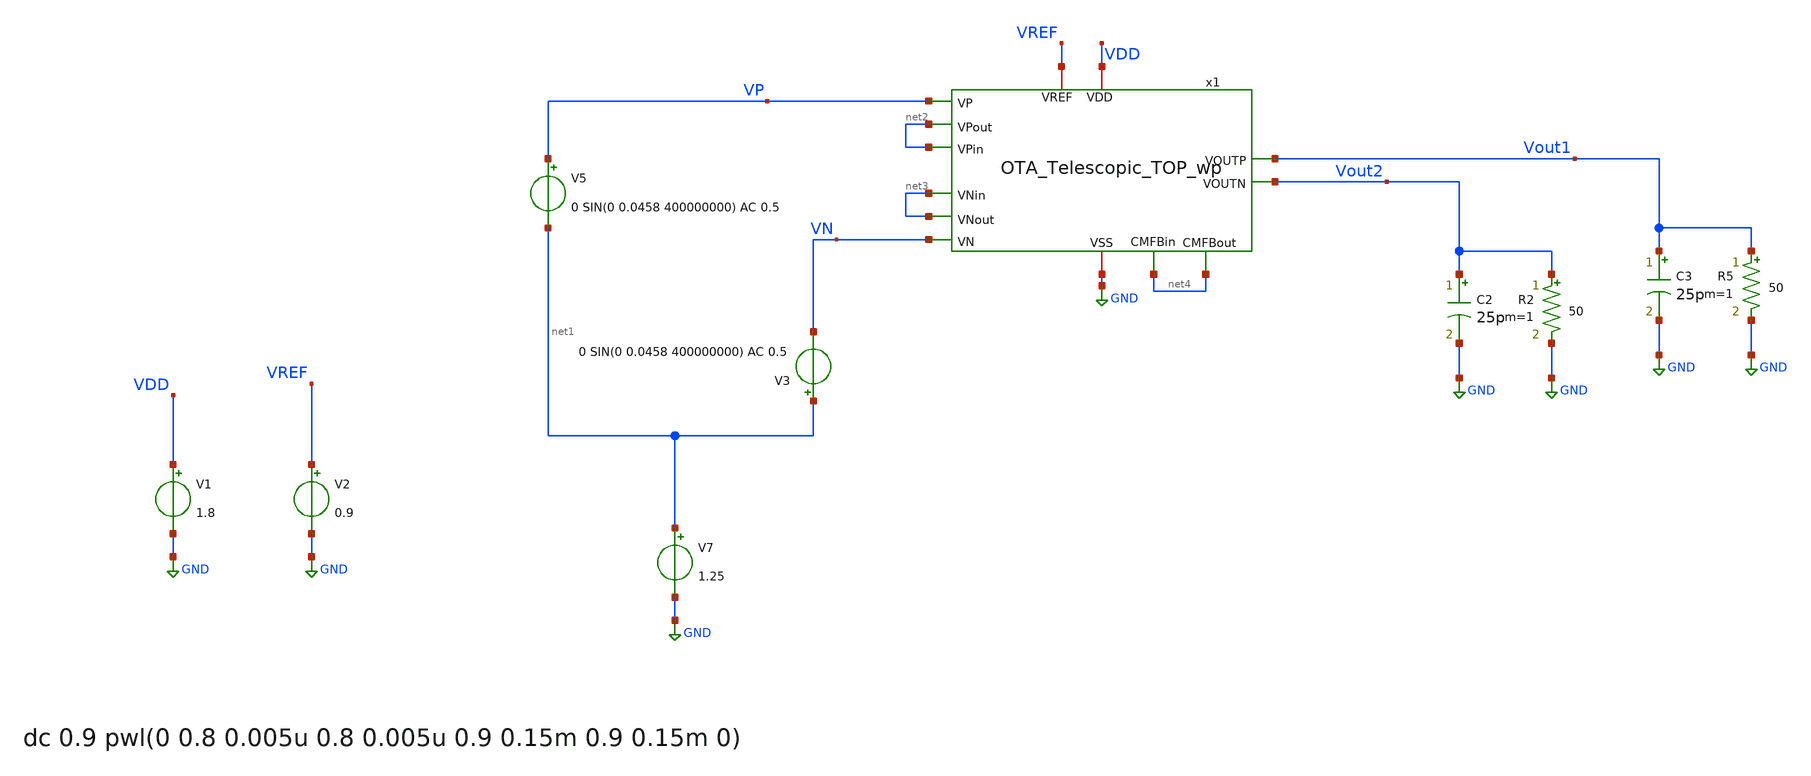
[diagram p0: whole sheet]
** sch_path: OTA_Telescopic/Testbenchs/OTA_Telescopic_TOP_TB_CL.sch
**.subckt OTA_Telescopic_TOP_TB_CL
V7 net1 GND 1.25
V5 VP net1 0 SIN(0 0.0458 400000000) AC 0.5
V1 VDD GND 1.8
V2 VREF GND 0.9
V3 net1 VN 0 SIN(0 0.0458 400000000) AC 0.5
x1 VDD GND net2 net2 Vout1 VP VN Vout2 net3 net3 net4 VREF net4 OTA_Telescopic_TOP_wp
C2 Vout2 GND 25p m=1
R2 Vout2 GND 50 m=1
C3 Vout1 GND 25p m=1
R5 Vout1 GND 50 m=1
**** begin user architecture code

** opencircuitdesign pdks install
.lib cornerMOSlv.lib mos_tt
.lib cornerRES.lib res_typ
.lib cornerCAP.lib cap_typ
.temp 65




.control
 set color0 = white

set wr_singlescale
set wr_vecnames

save all
tran 0.6103515625p 250n
*write NMOS_diode_large_signal.raw

let Vout1 = v(Vout1)
let Vout2 = v(Vout2)
let Vin = v(VP)-v(VN)

let Vout = v(Vout1)-v(Vout2)
wrdata Vout_tt_400.txt Vout
wrdata Vin_tt_400.txt Vin

plot Vin Vout
plot Vout1 Vout2
plot v(VP)-v(VN)
*plot v(VP) v(VN)

let Vo1 = v(x1.Vo1)
let Vo2 = v(x1.Vo2)

let Vo = Vo1-Vo2

wrdata Vo Vo

reset
noise v(Vout1) V5 dec 100 1 0.5e9 1
setplot noise1
*plot onoise_spectrum
setplot noise2
print onoise_total

.endc


**** end user architecture code
**.ends
.GLOBAL GND
.end
